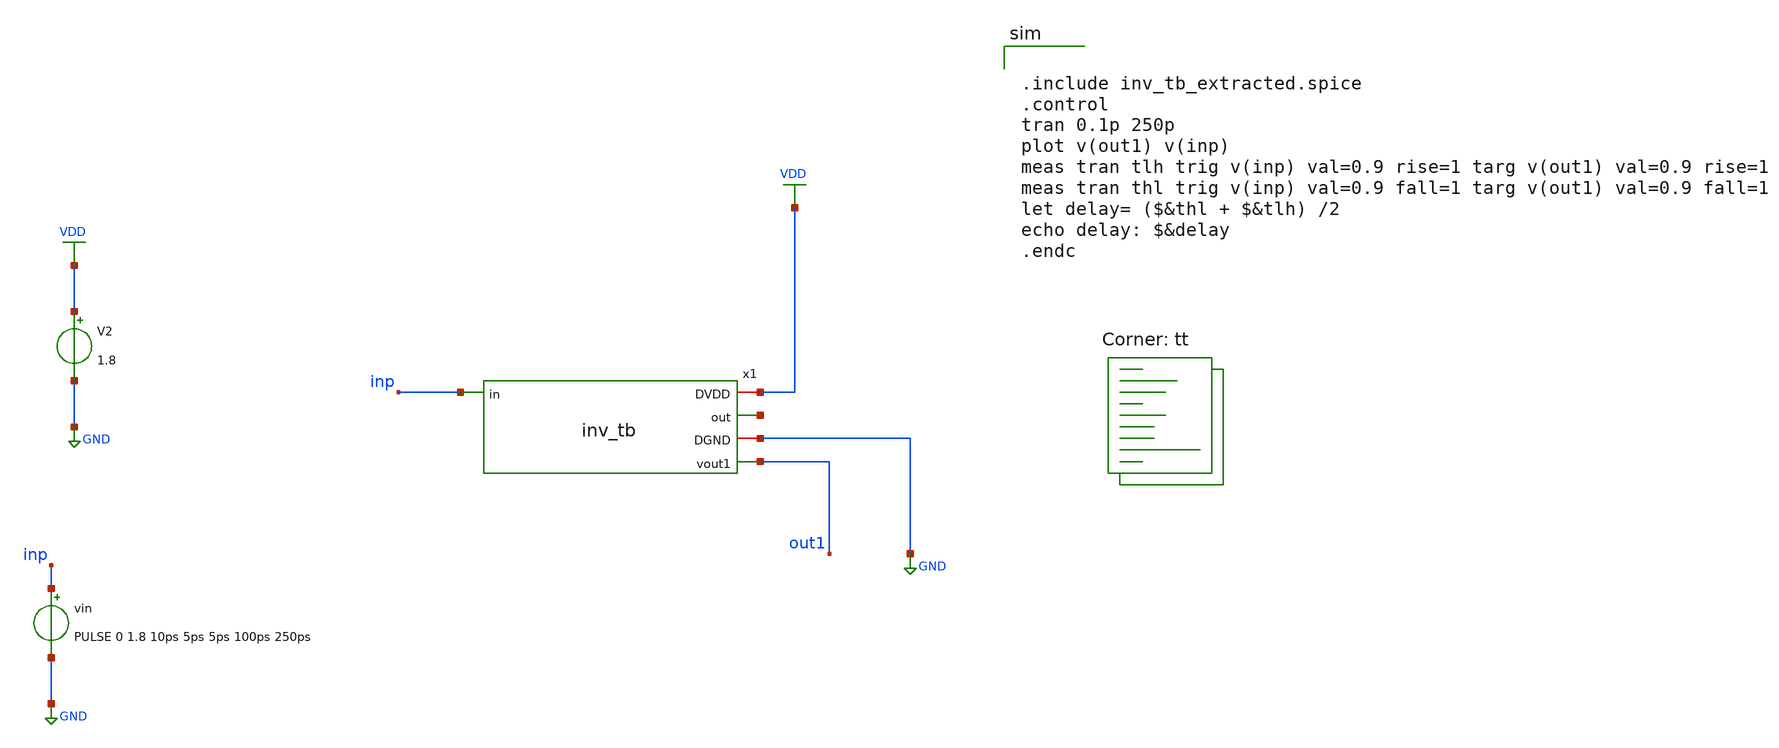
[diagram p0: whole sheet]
** sch_path: assignments/assignment4/assign1b.sch
**.subckt assign1b
vin inp GND PULSE 0 1.8 10ps 5ps 5ps 100ps 250ps
V2 VDD GND 1.8
x1 VDD net1 inp GND out1 inv_tb
**** begin user architecture code


.include inv_tb_extracted.spice
.control
tran 0.1p 250p
plot v(out1) v(inp)
meas tran tlh trig v(inp) val=0.9 rise=1 targ v(out1) val=0.9 rise=1
meas tran thl trig v(inp) val=0.9 fall=1 targ v(out1) val=0.9 fall=1
let delay= ($&thl + $&tlh) /2
echo delay: $&delay
.endc


.lib $::SKYWATER_MODELS/sky130.lib.spice tt
**** end user architecture code
**.ends

* expanding   symbol:  inv_tb.sym # of pins=5
** sym_path: assignments/assignment4/inv_tb.sym
** sch_path: assignments/assignment4/inv_tb.sch
.subckt inv_tb DVDD out in DGND vout1
*.iopin DGND
*.ipin in
*.opin out
*.iopin DVDD
*.opin vout1
x1 DVDD in vout1 DGND inv
x2 DVDD vout1 out DGND inv
.ends


* expanding   symbol:  inv.sym # of pins=8
** sym_path: assignments/assignment4/inv.sym
** sch_path: assignments/assignment4/inv.sch
.subckt inv DVDD in out DGND
*.ipin in
*.opin out
*.iopin DVDD
*.iopin DGND
XM3 out in DVDD DVDD sky130_fd_pr__pfet_01v8 L=0.15 W=0.84 nf=1 ad='int((nf+1)/2) * W/nf * 0.29' as='int((nf+2)/2) * W/nf * 0.29'
+ pd='2*int((nf+1)/2) * (W/nf + 0.29)' ps='2*int((nf+2)/2) * (W/nf + 0.29)' nrd='0.29 / W' nrs='0.29 / W'
+ sa=0 sb=0 sd=0 mult=1 m=1
XM2 out in DGND DGND sky130_fd_pr__nfet_01v8 L=0.15 W=0.42 nf=1 ad='int((nf+1)/2) * W/nf * 0.29' as='int((nf+2)/2) * W/nf * 0.29'
+ pd='2*int((nf+1)/2) * (W/nf + 0.29)' ps='2*int((nf+2)/2) * (W/nf + 0.29)' nrd='0.29 / W' nrs='0.29 / W'
+ sa=0 sb=0 sd=0 mult=1 m=1
.ends

.GLOBAL GND
.GLOBAL VDD
.end
